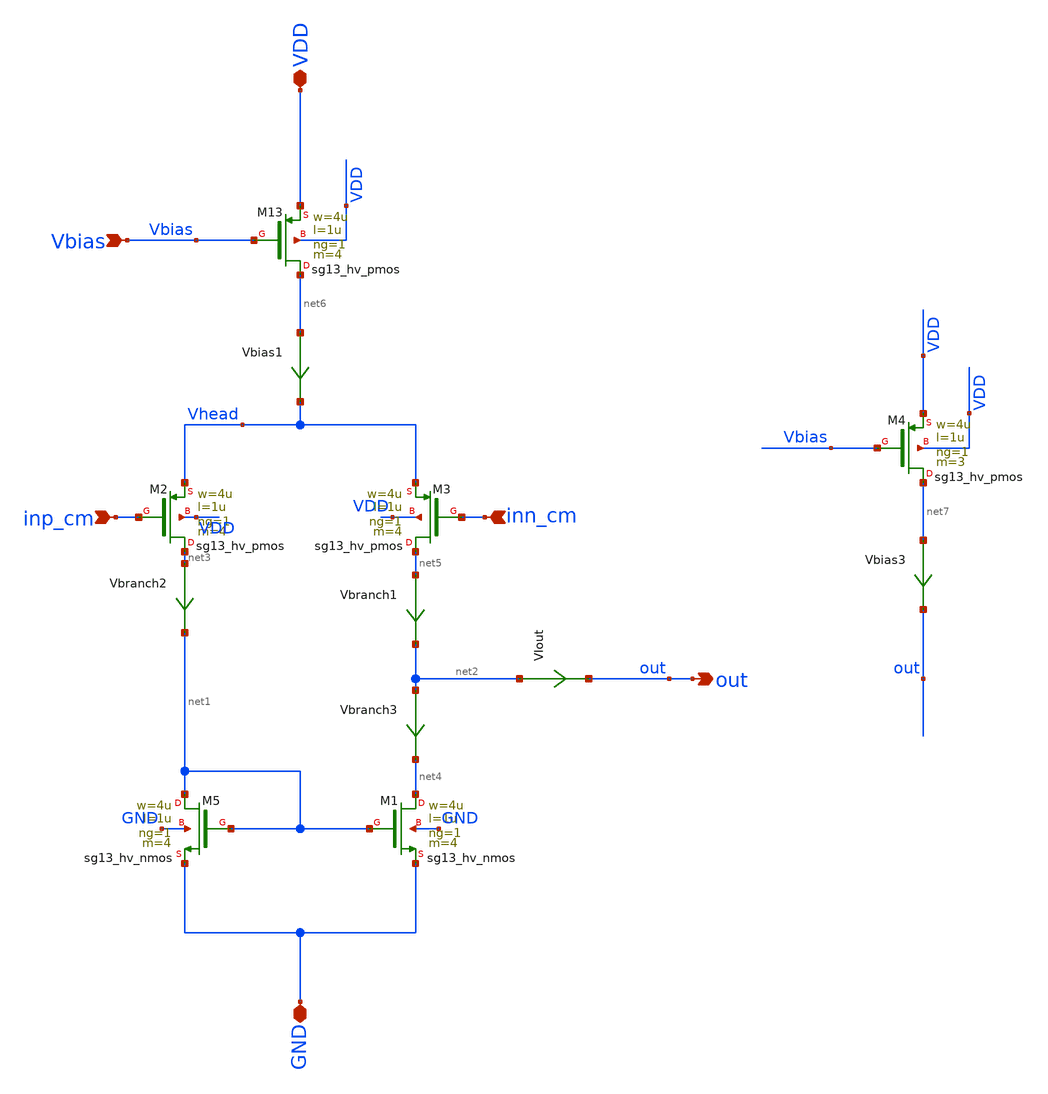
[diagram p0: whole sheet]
** sch_path: xschem/V2I_shift_final.sch
**.subckt V2I_shift_final inn_cm inp_cm out Vbias VDD GND
*.ipin inn_cm
*.ipin inp_cm
*.opin out
*.ipin Vbias
*.iopin VDD
*.iopin GND
VIout net2 out 0
.save i(viout)
XM2 net3 inp_cm Vhead VDD sg13_hv_pmos w=4u l=1u ng=1 m=4 mm_ok=1
XM5 net1 net1 GND GND sg13_hv_nmos w=4u l=1u ng=1 m=4 mm_ok=1
Vbias1 net6 Vhead 0
.save i(vbias1)
Vbranch1 net5 net2 0
.save i(vbranch1)
Vbranch2 net3 net1 0
.save i(vbranch2)
Vbranch3 net2 net4 0
.save i(vbranch3)
XM13 net6 Vbias VDD VDD sg13_hv_pmos w=4u l=1u ng=1 m=4 mm_ok=1
XM1 net4 net1 GND GND sg13_hv_nmos w=4u l=1u ng=1 m=4 mm_ok=1
XM3 net5 inn_cm Vhead VDD sg13_hv_pmos w=4u l=1u ng=1 m=4 mm_ok=1
Vbias3 net7 out 0
.save i(vbias3)
XM4 net7 Vbias VDD VDD sg13_hv_pmos w=4u l=1u ng=1 m=3 mm_ok=1
**.ends
.end
